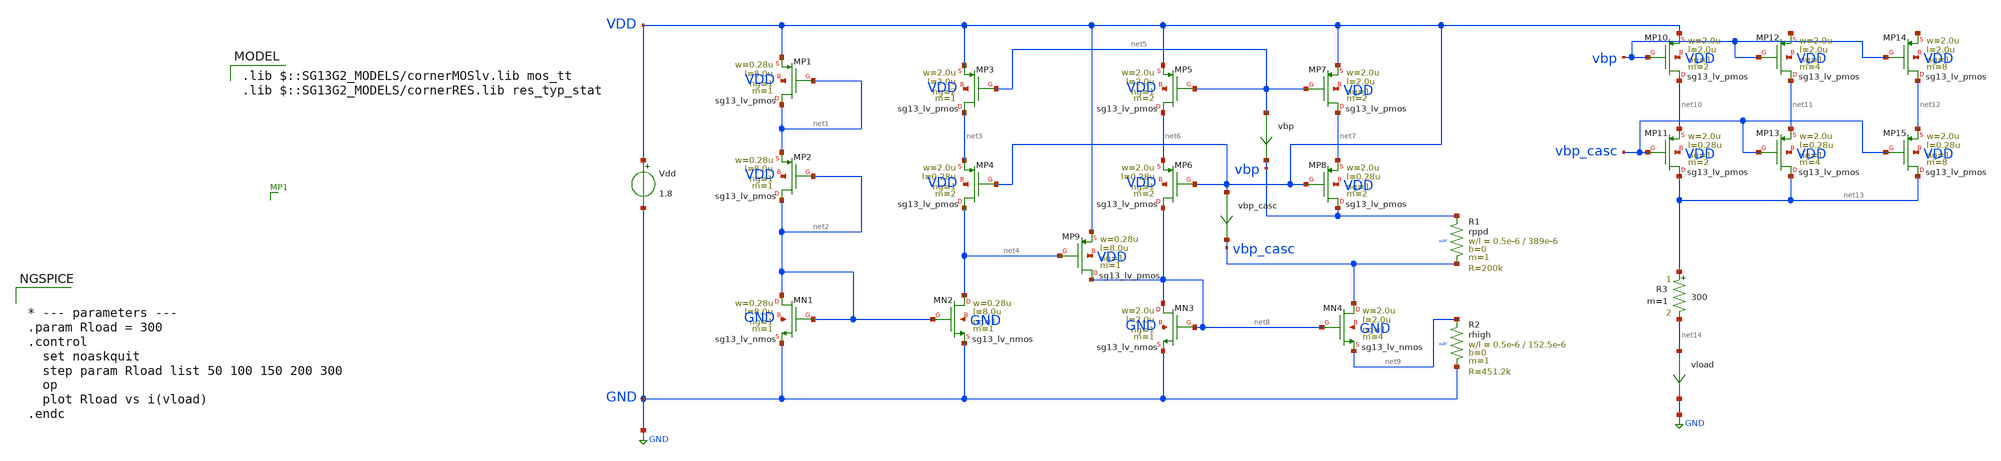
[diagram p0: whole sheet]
** sch_path: blocks/composite/dpi_adexp_neuron/design_data/xschem/trimmer.sch
**.subckt trimmer
XMP1 net1 net1 VDD VDD sg13_lv_pmos w=0.28u l=8.0u ng=1 m=1 mm_ok=1
XMP2 net2 net2 net1 VDD sg13_lv_pmos w=0.28u l=8.0u ng=1 m=1 mm_ok=1
XMN2 net4 net2 GND GND sg13_lv_nmos w=0.28u l=8.0u ng=1 m=1 mm_ok=1
XMN1 net2 net2 GND GND sg13_lv_nmos w=0.28u l=8.0u ng=1 m=1 mm_ok=1
XMP3 net3 net5 VDD VDD sg13_lv_pmos w=2.0u l=2.0u ng=2 m=1 mm_ok=1
XMP4 net4 VDD net3 VDD sg13_lv_pmos w=2.0u l=0.28u ng=1 m=2 mm_ok=1
XMP5 net6 net5 VDD VDD sg13_lv_pmos w=2.0u l=2.0u ng=1 m=2 mm_ok=1
XMP6 net8 VDD net6 VDD sg13_lv_pmos w=2.0u l=0.28u ng=1 m=2 mm_ok=1
XMP7 net7 net5 VDD VDD sg13_lv_pmos w=2.0u l=2.0u ng=1 m=2 mm_ok=1
XMP8 vbp VDD net7 VDD sg13_lv_pmos w=2.0u l=0.28u ng=1 m=2 mm_ok=1
XMP9 net8 net4 VDD VDD sg13_lv_pmos w=0.28u l=8.0u ng=1 m=1 mm_ok=1
XMN3 net8 net8 GND GND sg13_lv_nmos w=2.0u l=2.0u ng=1 m=1 mm_ok=1
XMN4 vbp_casc net8 net9 GND sg13_lv_nmos w=2.0u l=2.0u ng=1 m=4 mm_ok=1
XR1 vbp vbp_casc sub! rppd w=0.5e-6 l=389e-6 m=1 b=0 mm_ok=1
XR2 net9 GND sub! rhigh w=0.5e-6 l=152.5e-6 m=1 b=0 mm_ok=1
vbp net5 vbp 0
.save i(vbp)
vbp_casc VDD vbp_casc 0
.save i(vbp_casc)
Vdd VDD GND 1.8
R3 net13 net14 300 m=1
XMP10 net10 vbp VDD VDD sg13_lv_pmos w=2.0u l=2.0u ng=1 m=2 mm_ok=1
XMP11 net13 vbp_casc net10 VDD sg13_lv_pmos w=2.0u l=0.28u ng=1 m=2 mm_ok=1
XMP12 net11 vbp net15 VDD sg13_lv_pmos w=2.0u l=2.0u ng=1 m=4 mm_ok=1
XMP13 net13 vbp_casc net11 VDD sg13_lv_pmos w=2.0u l=0.28u ng=1 m=4 mm_ok=1
XMP14 net12 vbp net16 VDD sg13_lv_pmos w=2.0u l=2.0u ng=1 m=8 mm_ok=1
XMP15 net13 vbp_casc net12 VDD sg13_lv_pmos w=2.0u l=0.28u ng=1 m=8 mm_ok=1
vload net14 GND 0
.save i(vload)
**** begin user architecture code


* --- parameters ---
.param Rload = 300
.control
  set noaskquit
  step param Rload list 50 100 150 200 300
  op
  plot Rload vs i(vload)
.endc



 .lib $::SG13G2_MODELS/cornerMOSlv.lib mos_tt
.lib $::SG13G2_MODELS/cornerRES.lib res_typ_stat

**** end user architecture code
**.ends
.GLOBAL GND
.end
